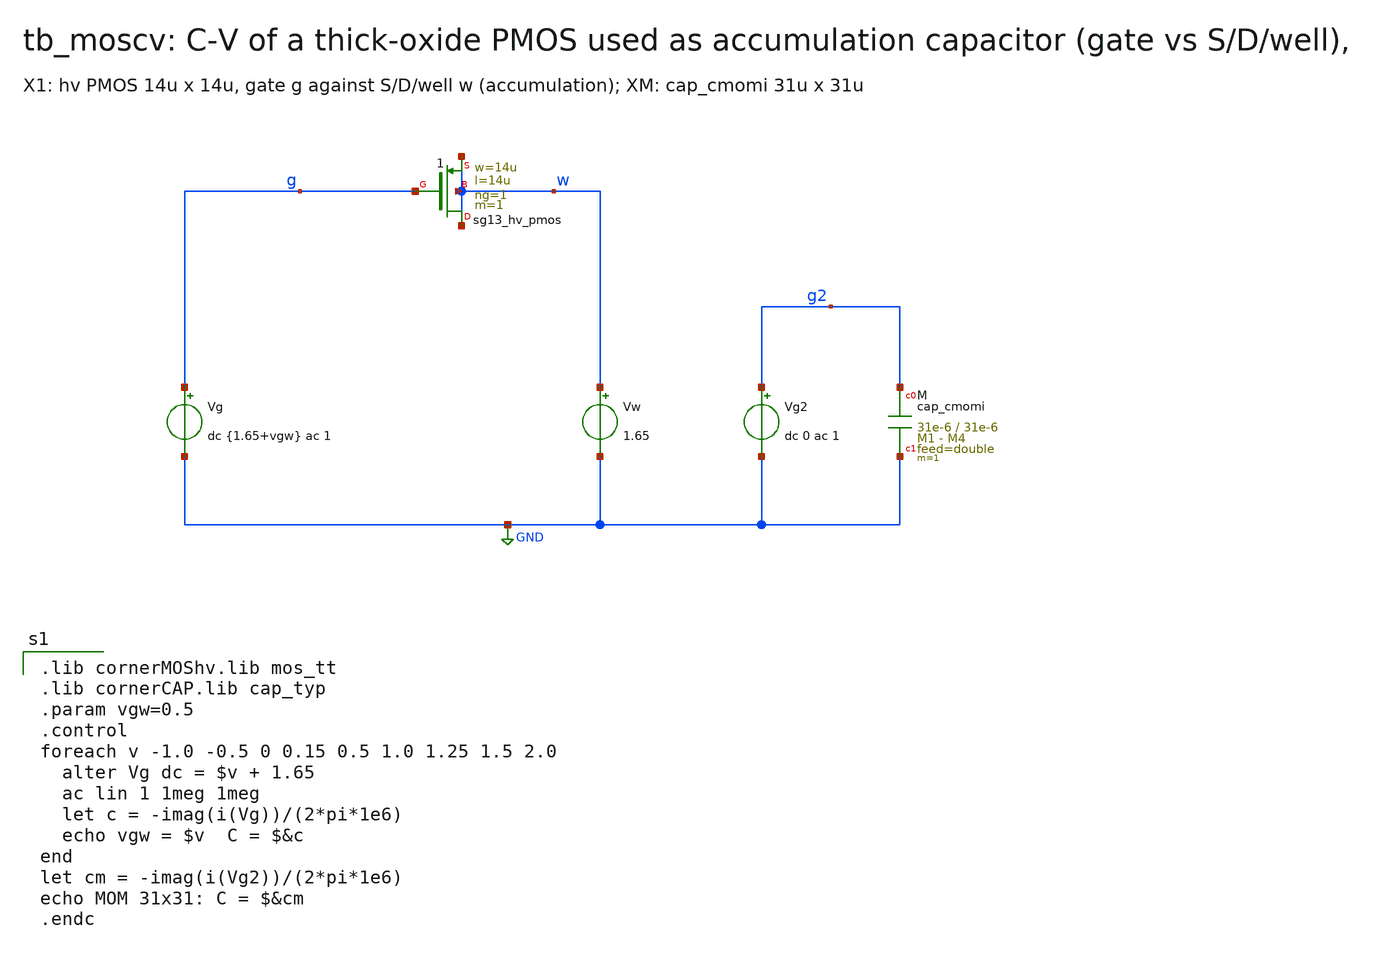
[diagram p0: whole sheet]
** sch_path: sudelbuecher/design_considerations/class_ab_pad_driver/improvements/xschem/tb_moscv.sch
**.subckt tb_moscv
Vg g GND dc {1.65+vgw} ac 1
X1 w g w w sg13_hv_pmos w=14u l=14u ng=1 m=1 mm_ok=1
Vw w GND 1.65
Vg2 g2 GND dc 0 ac 1
XM g2 GND cap_cmomi w=31e-6 l=31e-6 mmin=1 mmax=4 feed=double subblock=0 m=1 mm_ok=1
**** begin user architecture code

.lib cornerMOShv.lib mos_tt
.lib cornerCAP.lib cap_typ
.param vgw=0.5
.control
foreach v -1.0 -0.5 0 0.15 0.5 1.0 1.25 1.5 2.0
  alter Vg dc = $v + 1.65
  ac lin 1 1meg 1meg
  let c = -imag(i(Vg))/(2*pi*1e6)
  echo vgw = $v  C = $&c
end
let cm = -imag(i(Vg2))/(2*pi*1e6)
echo MOM 31x31: C = $&cm
.endc

**** end user architecture code
**.ends
.GLOBAL GND
.end
